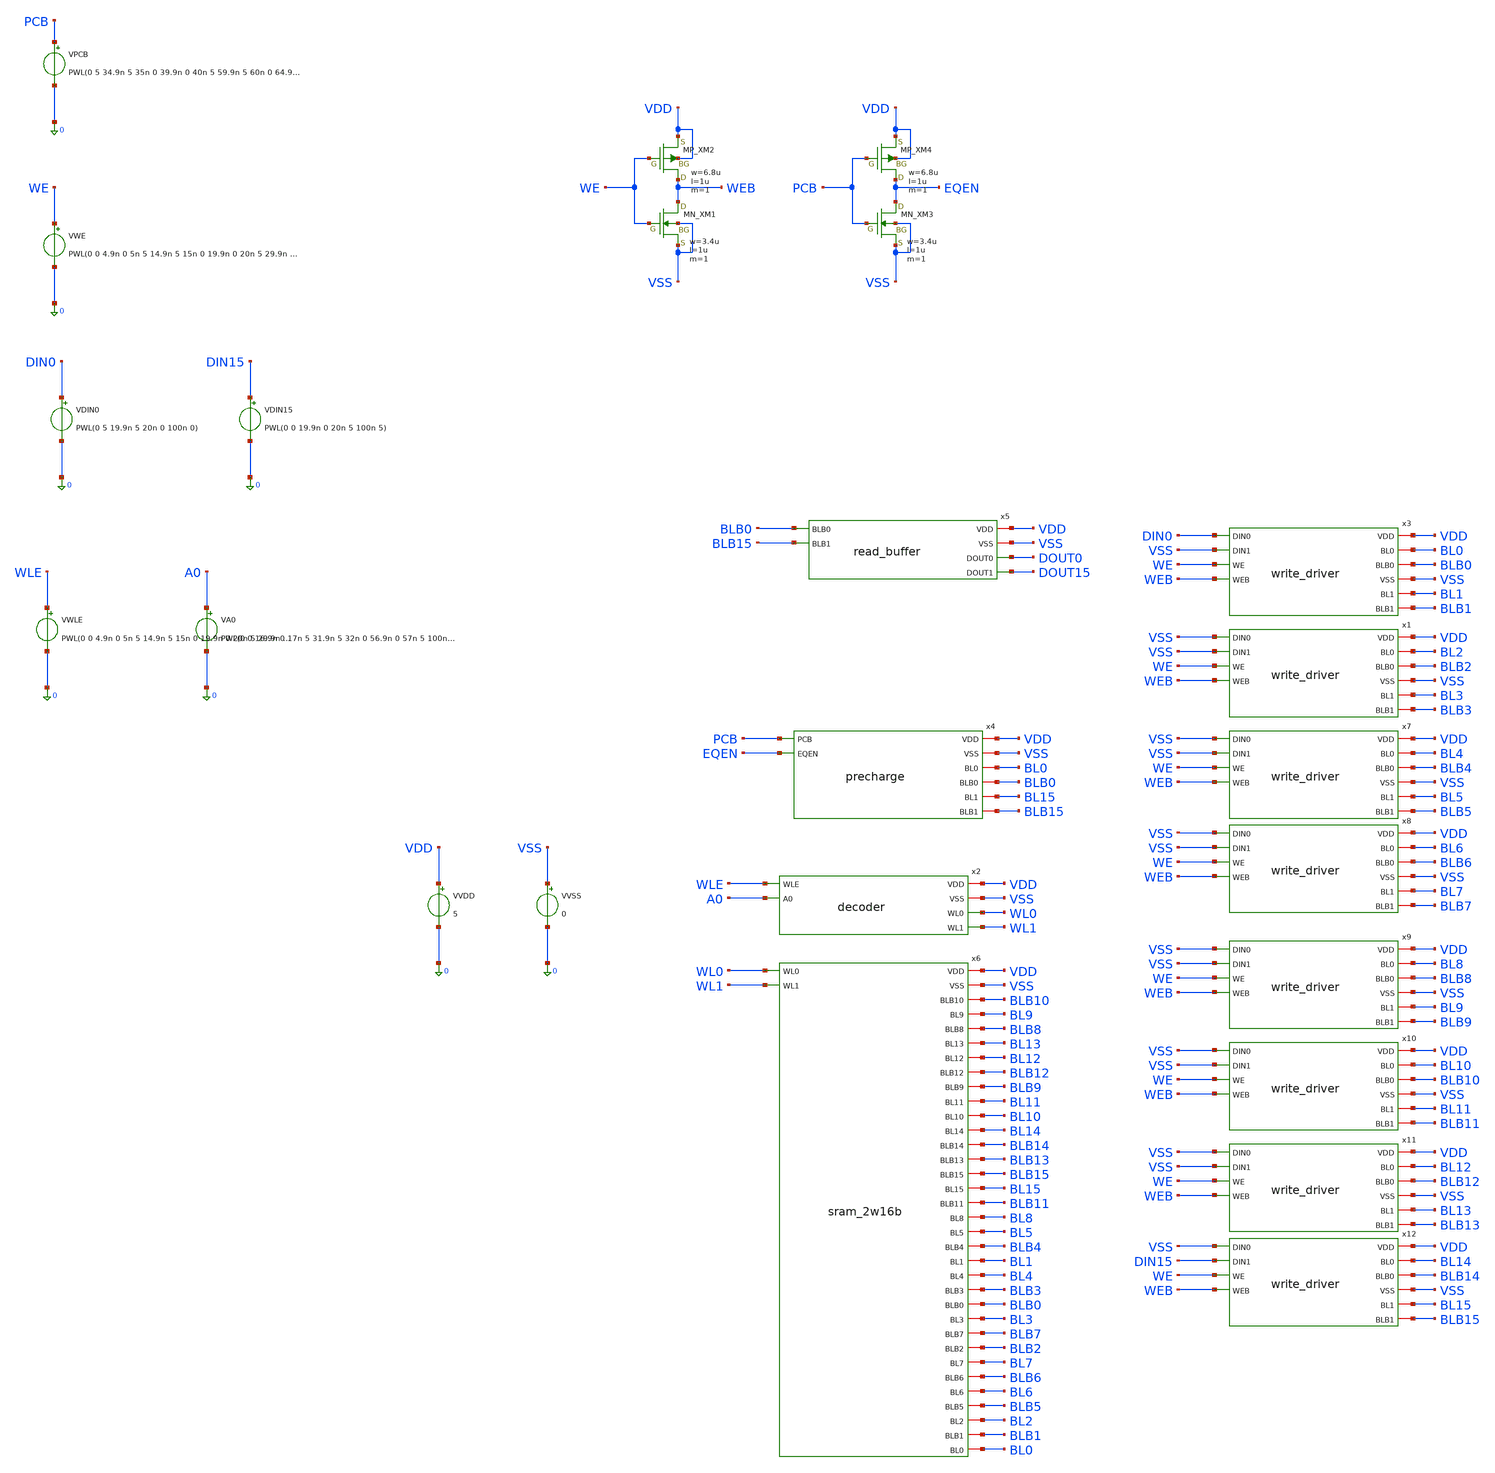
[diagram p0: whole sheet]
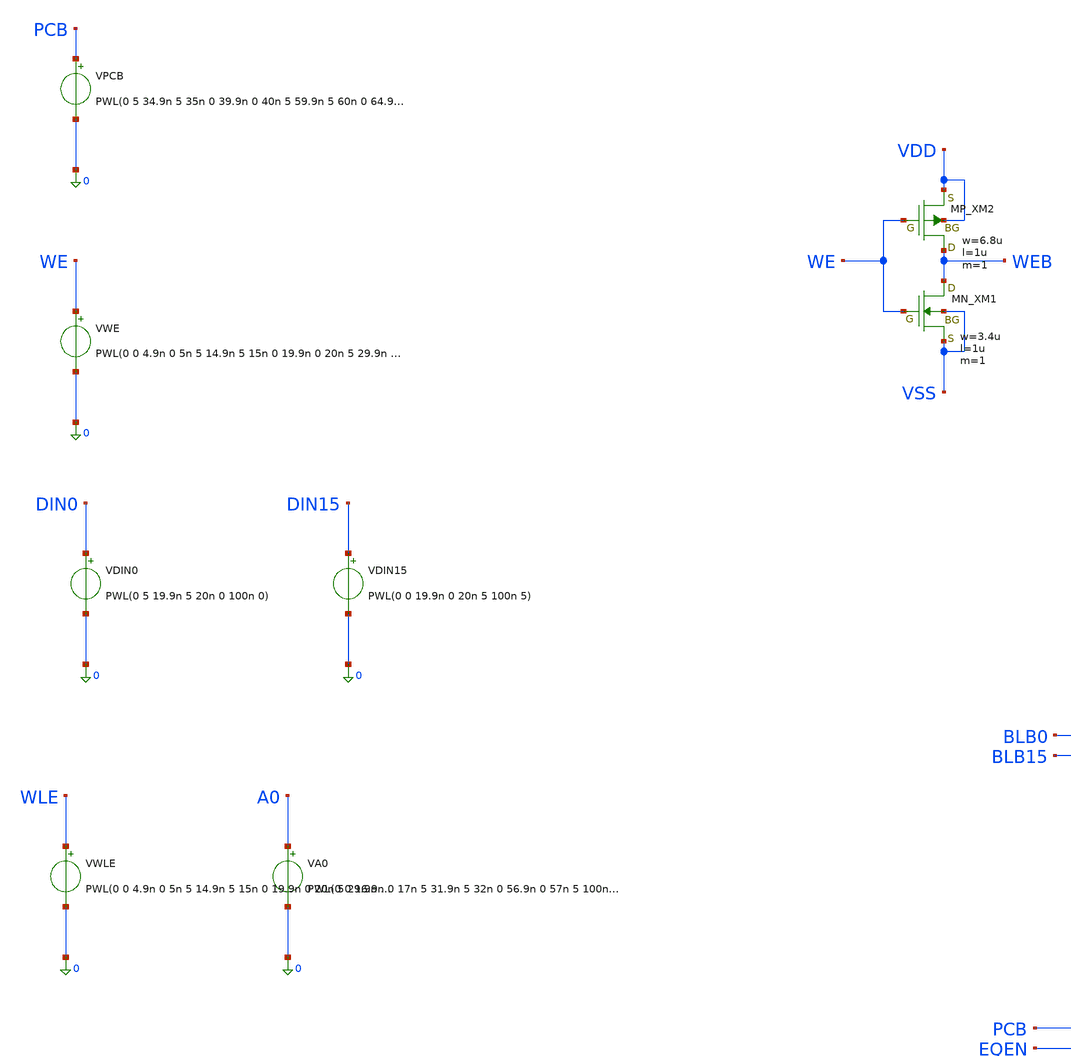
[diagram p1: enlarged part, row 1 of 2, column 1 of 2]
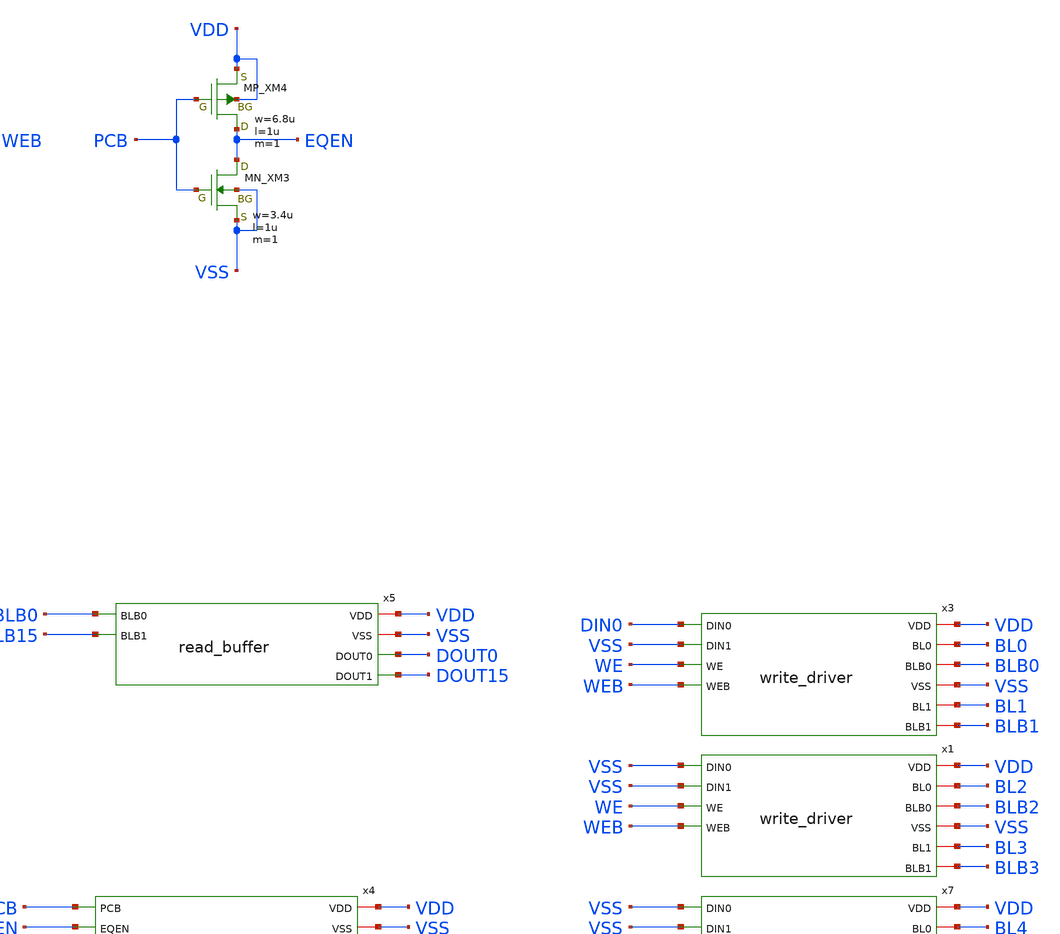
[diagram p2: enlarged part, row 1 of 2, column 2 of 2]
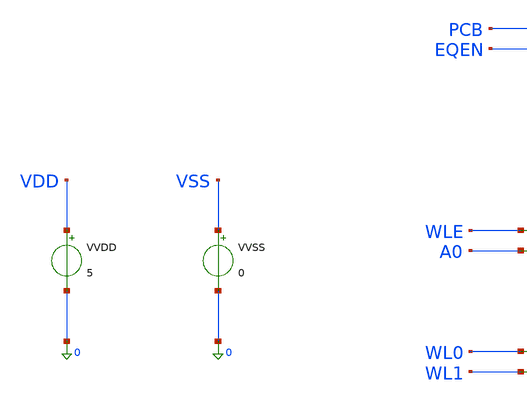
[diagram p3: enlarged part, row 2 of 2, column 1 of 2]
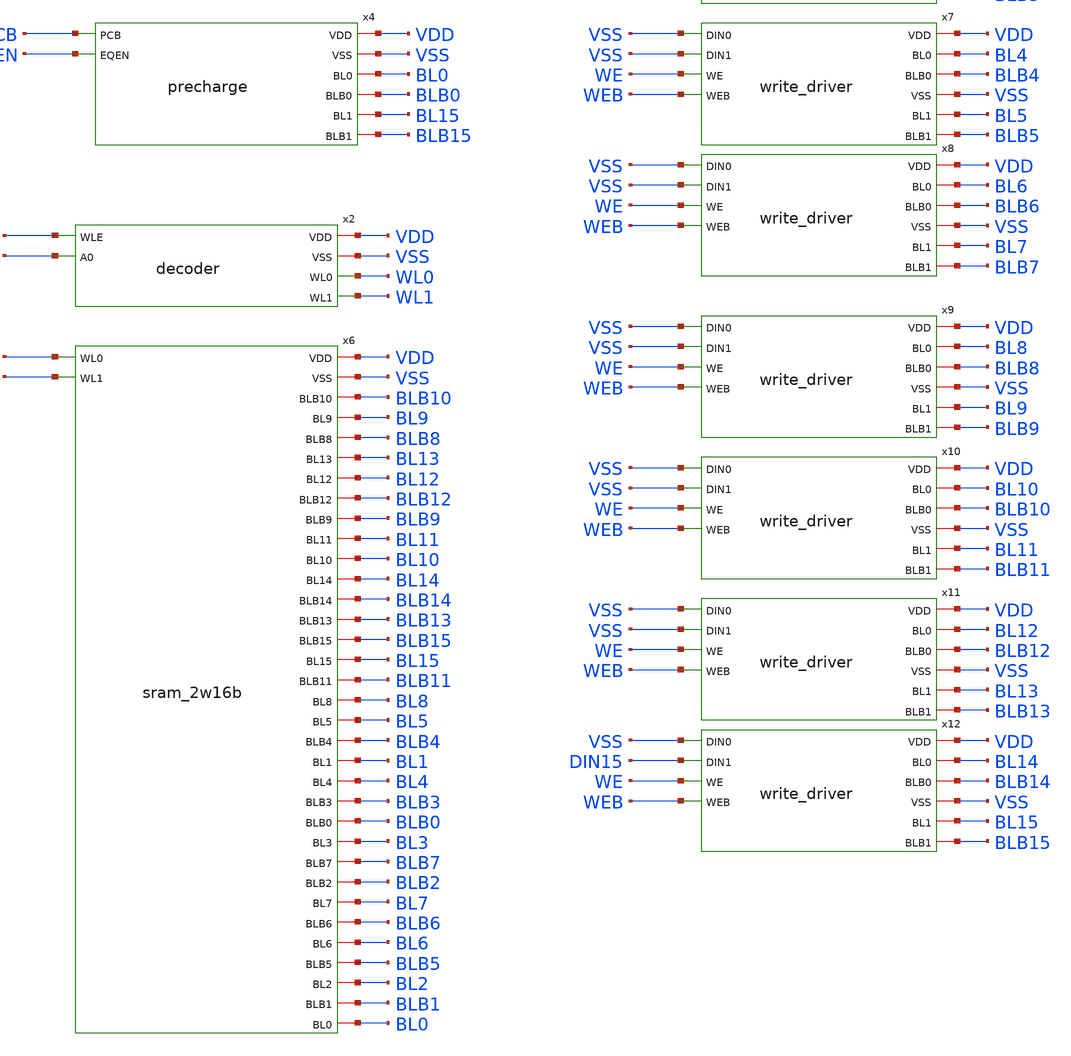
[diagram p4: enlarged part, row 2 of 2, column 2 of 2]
** sch_path: sram/tb_sram_2w16b.sch
**.subckt tb_sram_2w16b
VVDD VDD 0 5
VDIN0 DIN0 0 PWL(0 5 19.9n 5 20n 0 100n 0)
VVSS VSS 0 0
VWE WE 0 PWL(0 0 4.9n 0 5n 5 14.9n 5 15n 0 19.9n 0 20n 5 29.9n 5 30n 0 100n 0)
VPCB PCB 0 PWL(0 5 34.9n 5 35n 0 39.9n 0 40n 5 59.9n 5 60n 0 64.9n 0 65n 5 100n 5)
x2 VDD VSS WL0 WLE A0 WL1 decoder
VWLE WLE 0 PWL(0 0 4.9n 0 5n 5 14.9n 5 15n 0 19.9n 0 20n 5 29.9n 5 30n 0 44.9n 0 45n 5 54.9n 5 55n 0
+ 69.9n 0 70n 5 79.9n 5 80n 0 100n 0)
VA0 A0 0 PWL(0 0 16.9n 0 17n 5 31.9n 5 32n 0 56.9n 0 57n 5 100n 5)
x3 DIN0 VDD BL0 BLB0 VSS VSS BL1 WE BLB1 WEB write_driver
VDIN15 DIN15 0 PWL(0 0 19.9n 0 20n 5 100n 5)
x4 VDD VSS PCB EQEN BL0 BLB0 BL15 BLB15 precharge
x5 VDD VSS BLB0 BLB15 DOUT0 DOUT15 read_buffer
XXM1 WEB WE VSS VSS NMOS w=3.4u l=1u nrd=0 nrs=0 m=1
XXM2 WEB WE VDD VDD PMOS w=6.8u l=1u nrd=0 nrs=0 m=1
XXM3 EQEN PCB VSS VSS NMOS w=3.4u l=1u nrd=0 nrs=0 m=1
XXM4 EQEN PCB VDD VDD PMOS w=6.8u l=1u nrd=0 nrs=0 m=1
x1 VSS VDD BL2 BLB2 VSS VSS BL3 WE BLB3 WEB write_driver
x7 VSS VDD BL4 BLB4 VSS VSS BL5 WE BLB5 WEB write_driver
x8 VSS VDD BL6 BLB6 VSS VSS BL7 WE BLB7 WEB write_driver
x6 WL0 VDD VSS WL1 BLB10 BL9 BLB8 BL13 BL12 BLB12 BLB9 BL11 BL10 BL14 BLB14 BLB13 BLB15 BL15 BLB11
+ BL8 BL5 BLB4 BL1 BL4 BLB3 BLB0 BL3 BLB7 BLB2 BL7 BLB6 BL6 BLB5 BL2 BLB1 BL0 sram_2w16b
x9 VSS VDD BL8 BLB8 VSS VSS BL9 WE BLB9 WEB write_driver
x10 VSS VDD BL10 BLB10 VSS VSS BL11 WE BLB11 WEB write_driver
x11 VSS VDD BL12 BLB12 VSS VSS BL13 WE BLB13 WEB write_driver
x12 VSS VDD BL14 BLB14 VSS DIN15 BL15 WE BLB15 WEB write_driver
**** begin user architecture code
 .include $::LIB/ip62_models


.tran 10p 100n

* ============================================================
* ColMax 2w16b SRAM Read Measurement
* Observe: bit0 and bit15
* ============================================================

* WL 50% crossing
.meas tran t_wl0_rise WHEN v(WL0)=2.5 RISE=2
.meas tran t_wl1_rise WHEN v(WL1)=2.5 RISE=1

* BL differential around WL0 +0.5ns
.meas tran dvbl0_05  FIND par('abs(v(BL0)-v(BLB0))')   AT=49.35n
.meas tran dvbl15_05 FIND par('abs(v(BL15)-v(BLB15))') AT=49.35n

* BL differential around WL0 +1.0ns
.meas tran dvbl0_10  FIND par('abs(v(BL0)-v(BLB0))')   AT=49.85n
.meas tran dvbl15_10 FIND par('abs(v(BL15)-v(BLB15))') AT=49.85n

* First 1V differential AFTER WL0 has started rising
.meas tran t_dvbl0_1v  WHEN par('abs(v(BL0)-v(BLB0))')=1.0 RISE=1 TD=48.85n
.meas tran t_dvbl15_1v WHEN par('abs(v(BL15)-v(BLB15))')=1.0 RISE=1 TD=48.85n

* Delay
.meas tran td_bl0  PARAM='t_dvbl0_1v-t_wl0_rise'
.meas tran td_bl15 PARAM='t_dvbl15_1v-t_wl0_rise'

.control
run

plot v(pcb) v(eqen)+6
plot v(wl0) v(wl1)+6
plot v(dout0) v(dout15)+6
plot v(bl0) v(blb0)
plot v(bl15) v(blb15)

.endc


**** end user architecture code
**.ends
.end
